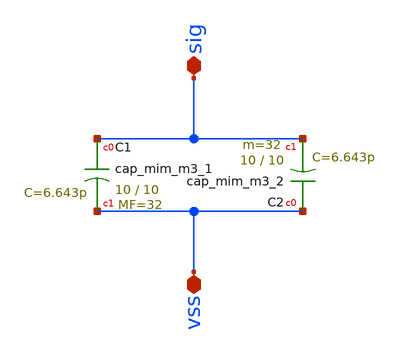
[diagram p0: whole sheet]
** sch_path: xschem/Switched_Caps/mim_cap_stacked_12pF.sch
**.subckt mim_cap_stacked_12pF sig vss
*.iopin sig
*.iopin vss
XC1 sig vss sky130_fd_pr__cap_mim_m3_1 W=10 L=10 MF=32 m=32
XC2 vss sig sky130_fd_pr__cap_mim_m3_2 W=10 L=10 MF=32 m=32
**.ends
.end
